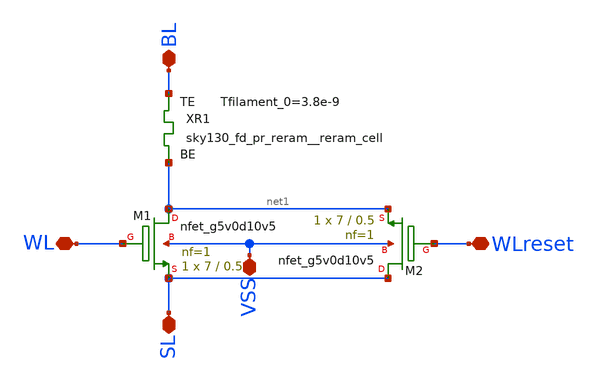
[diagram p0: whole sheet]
** sch_path: xschem/Crossbar/1T1R2.sch
* StefanSchippers/xschem_sky130/sky130_fd_pr/reram.sym:
* Copyright 2021 Stefan Frederik Schippers
* Licensed under the Apache License, Version 2.0 (the "License");
**.subckt 1T1R2 SL VSS WL BL WLreset
*.iopin SL
*.iopin VSS
*.iopin WL
*.iopin BL
*.iopin WLreset
XR1 BL net1 sky130_fd_pr_reram__reram_cell Tfilament_0=3.8e-9
XM1 net1 WL SL VSS sky130_fd_pr__nfet_g5v0d10v5 L=0.5 W=7 nf=1 ad='int((nf+1)/2) * W/nf * 0.29' as='int((nf+2)/2) * W/nf * 0.29'
+ pd='2*int((nf+1)/2) * (W/nf + 0.29)' ps='2*int((nf+2)/2) * (W/nf + 0.29)' nrd='0.29 / W' nrs='0.29 / W'
+ sa=0 sb=0 sd=0 mult=1 m=1
XM2 SL WLreset net1 VSS sky130_fd_pr__nfet_g5v0d10v5 L=0.5 W=7 nf=1 ad='int((nf+1)/2) * W/nf * 0.29'
+ as='int((nf+2)/2) * W/nf * 0.29' pd='2*int((nf+1)/2) * (W/nf + 0.29)' ps='2*int((nf+2)/2) * (W/nf + 0.29)'
+ nrd='0.29 / W' nrs='0.29 / W' sa=0 sb=0 sd=0 mult=1 m=1
**.ends
**** begin user architecture code

.subckt sky130_fd_pr_reram__reram_cell TE BE Tfilament_0=3.3e-9 area_ox=0.1024e-12
N1 TE BE nFilament sky130_fd_pr_reram__reram_model
.ic v(nFilament)={Tfilament_0*1.0e9}
.ends sky130_fd_pr_reram__reram_cell

.model sky130_fd_pr_reram__reram_model sky130_fd_pr_reram__reram_module  area_ox = 0.1024e-12  Tox =
+ 5.0  Tfilament_max = 4.9  Tfilament_min = 3.3  Eact_generation = 1.501  Eact_recombination  = 1.500
+  I_k1  = 6.140e-5  Tfilament_ref = 4.7249  V_ref = 0.430  velocity_k1 = 150  gamma_k0  = 16.5  gamma_k1
+  = -1.25  Temperature_0 = 300  C_thermal = 3.1825e-16  tau_thermal = 0.23e-9  t_step  = 1.0e-9
+  smoothing = 1e-7  Kclip = 200

.control
pre_osdi $SKYWATER_MODELS/sky130_fd_pr_reram__reram_module.osdi
.endc

**** end user architecture code
.end
